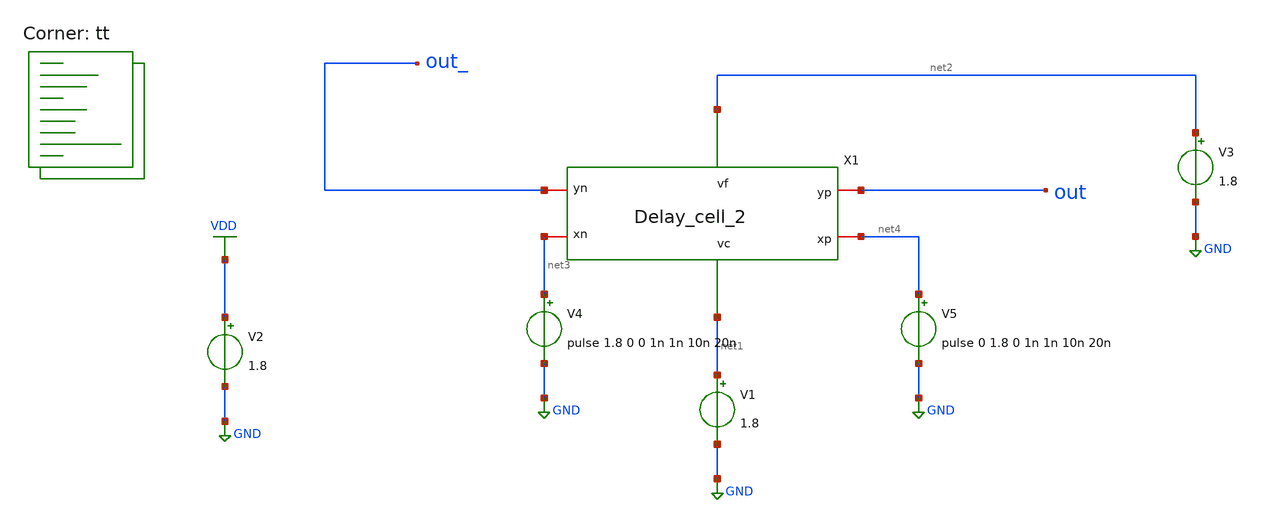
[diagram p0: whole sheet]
** sch_path: modified_cell_sym_test.sch
**.subckt modified_cell_sym_test
X1 out out_ net4 net3 net2 net1 Delay_cell_2
V2 VDD GND 1.8
V1 net1 GND 1.8
V3 net2 GND 1.8
V4 net3 GND pulse 1.8 0 0 1n 1n 10n 20n
V5 net4 GND pulse 0 1.8 0 1n 1n 10n 20n
**** begin user architecture code



.tran 1n 10u

.save all

.lib $::SKYWATER_MODELS/sky130.lib.spice tt
**** end user architecture code
**.ends

* expanding   symbol:  Delay_cell_2.sym # of pins=6
** sym_path: Delay_cell_2.sym
** sch_path: Delay_cell_2.sch
.subckt Delay_cell_2 yp yn xp xn vf vc
*.iopin yp
*.iopin xn
*.iopin xp
*.iopin yn
*.ipin vf
*.ipin vc
R2 yp net1 800 m=1
R1 yn net2 800 m=1
XM1 net1 xn GND GND sky130_fd_pr__nfet_01v8 L=0.15 W=6 nf=1 ad='int((nf+1)/2) * W/nf * 0.29' as='int((nf+2)/2) * W/nf * 0.29'
+ pd='2*int((nf+1)/2) * (W/nf + 0.29)' ps='2*int((nf+2)/2) * (W/nf + 0.29)' nrd='0.29 / W' nrs='0.29 / W'
+ sa=0 sb=0 sd=0 mult=1 m=1
XM2 net2 xp GND GND sky130_fd_pr__nfet_01v8 L=0.15 W=6 nf=1 ad='int((nf+1)/2) * W/nf * 0.29' as='int((nf+2)/2) * W/nf * 0.29'
+ pd='2*int((nf+1)/2) * (W/nf + 0.29)' ps='2*int((nf+2)/2) * (W/nf + 0.29)' nrd='0.29 / W' nrs='0.29 / W'
+ sa=0 sb=0 sd=0 mult=1 m=1
XM3 yn net1 VDD VDD sky130_fd_pr__pfet_01v8 L=0.15 W=1 nf=1 ad='int((nf+1)/2) * W/nf * 0.29' as='int((nf+2)/2) * W/nf * 0.29'
+ pd='2*int((nf+1)/2) * (W/nf + 0.29)' ps='2*int((nf+2)/2) * (W/nf + 0.29)' nrd='0.29 / W' nrs='0.29 / W'
+ sa=0 sb=0 sd=0 mult=1 m=1
XM4 yp vc VDD VDD sky130_fd_pr__pfet_01v8 L=0.15 W=1 nf=1 ad='int((nf+1)/2) * W/nf * 0.29' as='int((nf+2)/2) * W/nf * 0.29'
+ pd='2*int((nf+1)/2) * (W/nf + 0.29)' ps='2*int((nf+2)/2) * (W/nf + 0.29)' nrd='0.29 / W' nrs='0.29 / W'
+ sa=0 sb=0 sd=0 mult=1 m=1
XM5 yp vf VDD VDD sky130_fd_pr__pfet_01v8 L=0.15 W=1 nf=1 ad='int((nf+1)/2) * W/nf * 0.29' as='int((nf+2)/2) * W/nf * 0.29'
+ pd='2*int((nf+1)/2) * (W/nf + 0.29)' ps='2*int((nf+2)/2) * (W/nf + 0.29)' nrd='0.29 / W' nrs='0.29 / W'
+ sa=0 sb=0 sd=0 mult=1 m=1
XM6 yp net2 VDD VDD sky130_fd_pr__pfet_01v8 L=0.15 W=1 nf=1 ad='int((nf+1)/2) * W/nf * 0.29' as='int((nf+2)/2) * W/nf * 0.29'
+ pd='2*int((nf+1)/2) * (W/nf + 0.29)' ps='2*int((nf+2)/2) * (W/nf + 0.29)' nrd='0.29 / W' nrs='0.29 / W'
+ sa=0 sb=0 sd=0 mult=1 m=1
XM7 yn vf VDD VDD sky130_fd_pr__pfet_01v8 L=0.15 W=1 nf=1 ad='int((nf+1)/2) * W/nf * 0.29' as='int((nf+2)/2) * W/nf * 0.29'
+ pd='2*int((nf+1)/2) * (W/nf + 0.29)' ps='2*int((nf+2)/2) * (W/nf + 0.29)' nrd='0.29 / W' nrs='0.29 / W'
+ sa=0 sb=0 sd=0 mult=1 m=1
XM8 yn vc VDD VDD sky130_fd_pr__pfet_01v8 L=0.15 W=1 nf=1 ad='int((nf+1)/2) * W/nf * 0.29' as='int((nf+2)/2) * W/nf * 0.29'
+ pd='2*int((nf+1)/2) * (W/nf + 0.29)' ps='2*int((nf+2)/2) * (W/nf + 0.29)' nrd='0.29 / W' nrs='0.29 / W'
+ sa=0 sb=0 sd=0 mult=1 m=1
.ends

.GLOBAL VDD
.GLOBAL GND
.end
